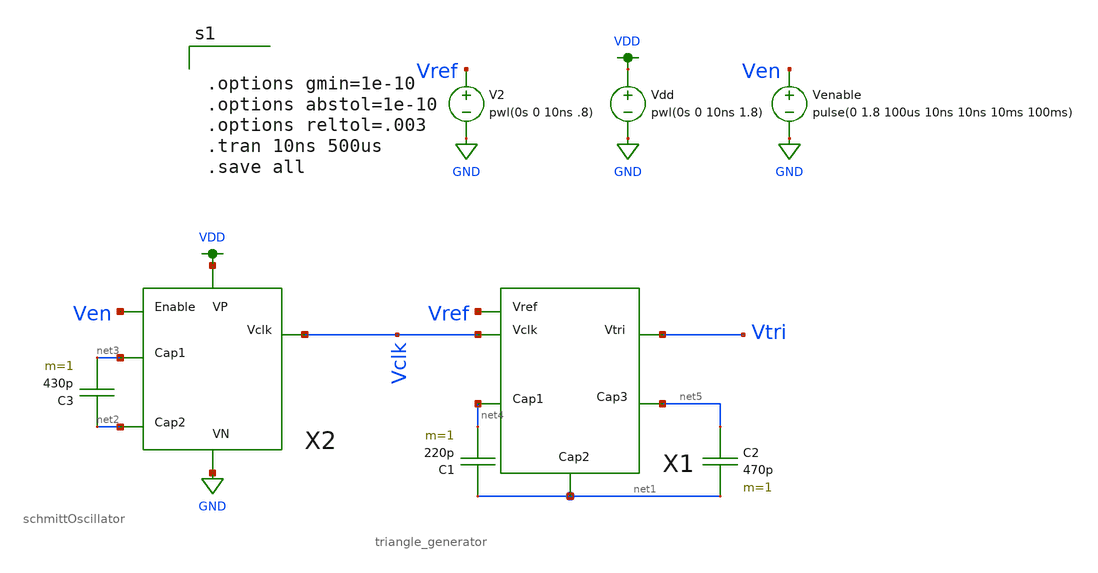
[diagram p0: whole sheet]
** sch_path: schematics/old/triangle_generator_testbench.sch
**.subckt triangle_generator_testbench
Vdd VDD GND pwl(0s 0 10ns 1.8)
V2 Vref GND pwl(0s 0 10ns .8)
X1 Vtri Vref net4 Vclk net1 net5 triangle_generator
C1 net1 net4 220p m=1
C2 net5 net1 470p m=1
X2 Ven net3 net2 VDD GND Vclk schmittOscillator
C3 net2 net3 430p m=1
Venable Ven GND pulse(0 1.8 100us 10ns 10ns 10ms 100ms)
**** begin user architecture code


.options gmin=1e-10
.options abstol=1e-10
.options reltol=.003
.tran 10ns 500us
.save all


.option wnflag=1
.param MC_SWITCH=0.0
.lib ~/skywater/skywater-pdk/libraries/sky130_fd_pr_ngspice/latest/models/sky130.lib.spice tt

**** end user architecture code
**.ends
.GLOBAL GND
.GLOBAL VDD
.end
